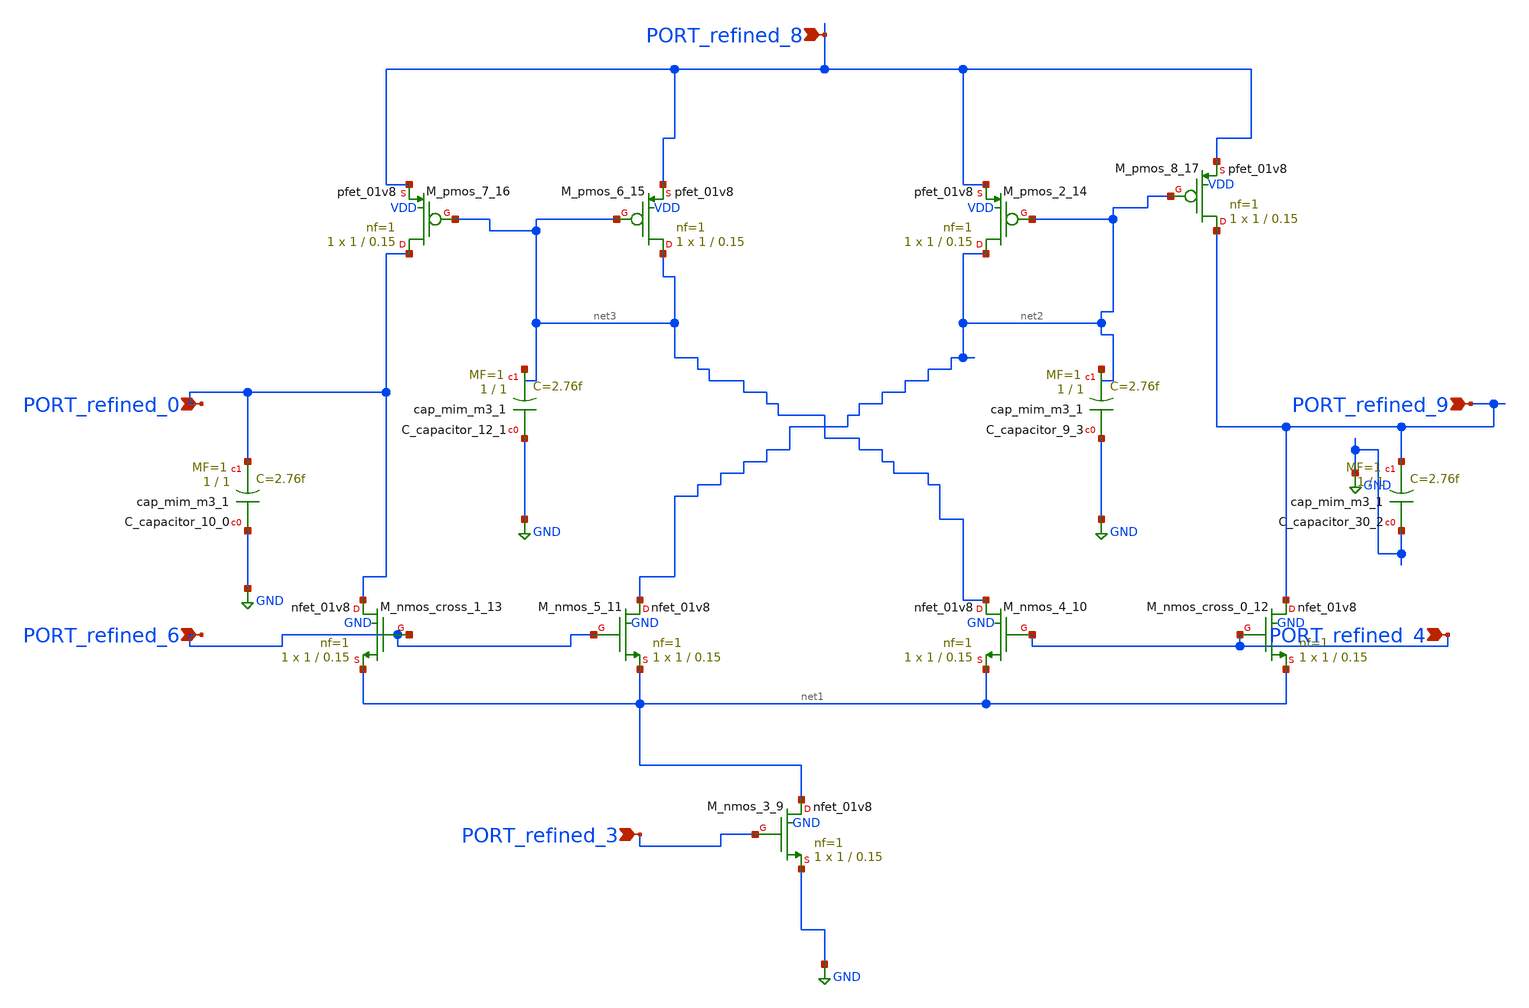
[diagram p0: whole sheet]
** sch_path: schematics/Image2Net/035.sch
**.subckt 035 PORT_refined_4 PORT_refined_9 PORT_refined_0 PORT_refined_6 PORT_refined_8
*+ PORT_refined_3
*.ipin PORT_refined_4
*.ipin PORT_refined_9
*.ipin PORT_refined_0
*.ipin PORT_refined_6
*.ipin PORT_refined_8
*.ipin PORT_refined_3
XC_capacitor_10_0 GND PORT_refined_0 sky130_fd_pr__cap_mim_m3_1 W=1 L=1 MF=1 m=1
XC_capacitor_12_1 GND net3 sky130_fd_pr__cap_mim_m3_1 W=1 L=1 MF=1 m=1
XC_capacitor_30_2 GND PORT_refined_9 sky130_fd_pr__cap_mim_m3_1 W=1 L=1 MF=1 m=1
XC_capacitor_9_3 GND net2 sky130_fd_pr__cap_mim_m3_1 W=1 L=1 MF=1 m=1
XM_nmos_3_9 net1 PORT_refined_3 GND GND sky130_fd_pr__nfet_01v8 L=0.15 W=1 nf=1 ad='int((1 + 1)/2) * 1 / 1 * 0.29'
+ as='int((1 + 2)/2) * 1 / 1 * 0.29' pd='2*int((1 + 1)/2) * (1 / 1 + 0.29)' ps='2*int((1 + 2)/2) * (1 / 1 + 0.29)'
+ nrd='0.29 / 1 ' nrs='0.29 / 1 ' sa=0 sb=0 sd=0 mult=1 m=1
XM_nmos_4_10 net3 PORT_refined_4 net1 GND sky130_fd_pr__nfet_01v8 L=0.15 W=1 nf=1 ad='int((1 + 1)/2) * 1 / 1 * 0.29'
+ as='int((1 + 2)/2) * 1 / 1 * 0.29' pd='2*int((1 + 1)/2) * (1 / 1 + 0.29)' ps='2*int((1 + 2)/2) * (1 / 1 + 0.29)'
+ nrd='0.29 / 1 ' nrs='0.29 / 1 ' sa=0 sb=0 sd=0 mult=1 m=1
XM_nmos_5_11 net2 PORT_refined_6 net1 GND sky130_fd_pr__nfet_01v8 L=0.15 W=1 nf=1 ad='int((1 + 1)/2) * 1 / 1 * 0.29'
+ as='int((1 + 2)/2) * 1 / 1 * 0.29' pd='2*int((1 + 1)/2) * (1 / 1 + 0.29)' ps='2*int((1 + 2)/2) * (1 / 1 + 0.29)'
+ nrd='0.29 / 1 ' nrs='0.29 / 1 ' sa=0 sb=0 sd=0 mult=1 m=1
XM_nmos_cross_0_12 PORT_refined_9 PORT_refined_4 net1 GND sky130_fd_pr__nfet_01v8 L=0.15 W=1 nf=1 ad='int((1 + 1)/2) * 1 / 1 * 0.29'
+ as='int((1 + 2)/2) * 1 / 1 * 0.29' pd='2*int((1 + 1)/2) * (1 / 1 + 0.29)' ps='2*int((1 + 2)/2) * (1 / 1 + 0.29)'
+ nrd='0.29 / 1 ' nrs='0.29 / 1 ' sa=0 sb=0 sd=0 mult=1 m=1
XM_nmos_cross_1_13 PORT_refined_0 PORT_refined_6 net1 GND sky130_fd_pr__nfet_01v8 L=0.15 W=1 nf=1 ad='int((1 + 1)/2) * 1 / 1 * 0.29'
+ as='int((1 + 2)/2) * 1 / 1 * 0.29' pd='2*int((1 + 1)/2) * (1 / 1 + 0.29)' ps='2*int((1 + 2)/2) * (1 / 1 + 0.29)'
+ nrd='0.29 / 1 ' nrs='0.29 / 1 ' sa=0 sb=0 sd=0 mult=1 m=1
XM_pmos_2_14 net2 net2 PORT_refined_8 VDD sky130_fd_pr__pfet_01v8 L=0.15 W=1 nf=1 ad='int((1 + 1)/2) * 1 / 1 * 0.29'
+ as='int((1 + 2)/2) * 1 / 1 * 0.29' pd='2*int((1 + 1)/2) * (1 / 1 + 0.29)' ps='2*int((1 + 2)/2) * (1 / 1 + 0.29)'
+ nrd='0.29 / 1 ' nrs='0.29 / 1 ' sa=0 sb=0 sd=0 mult=1 m=1
XM_pmos_6_15 net3 net3 PORT_refined_8 VDD sky130_fd_pr__pfet_01v8 L=0.15 W=1 nf=1 ad='int((1 + 1)/2) * 1 / 1 * 0.29'
+ as='int((1 + 2)/2) * 1 / 1 * 0.29' pd='2*int((1 + 1)/2) * (1 / 1 + 0.29)' ps='2*int((1 + 2)/2) * (1 / 1 + 0.29)'
+ nrd='0.29 / 1 ' nrs='0.29 / 1 ' sa=0 sb=0 sd=0 mult=1 m=1
XM_pmos_7_16 PORT_refined_0 net3 PORT_refined_8 VDD sky130_fd_pr__pfet_01v8 L=0.15 W=1 nf=1 ad='int((1 + 1)/2) * 1 / 1 * 0.29'
+ as='int((1 + 2)/2) * 1 / 1 * 0.29' pd='2*int((1 + 1)/2) * (1 / 1 + 0.29)' ps='2*int((1 + 2)/2) * (1 / 1 + 0.29)'
+ nrd='0.29 / 1 ' nrs='0.29 / 1 ' sa=0 sb=0 sd=0 mult=1 m=1
XM_pmos_8_17 PORT_refined_9 net2 PORT_refined_8 VDD sky130_fd_pr__pfet_01v8 L=0.15 W=1 nf=1 ad='int((1 + 1)/2) * 1 / 1 * 0.29'
+ as='int((1 + 2)/2) * 1 / 1 * 0.29' pd='2*int((1 + 1)/2) * (1 / 1 + 0.29)' ps='2*int((1 + 2)/2) * (1 / 1 + 0.29)'
+ nrd='0.29 / 1 ' nrs='0.29 / 1 ' sa=0 sb=0 sd=0 mult=1 m=1
**.ends
.GLOBAL GND
.end
